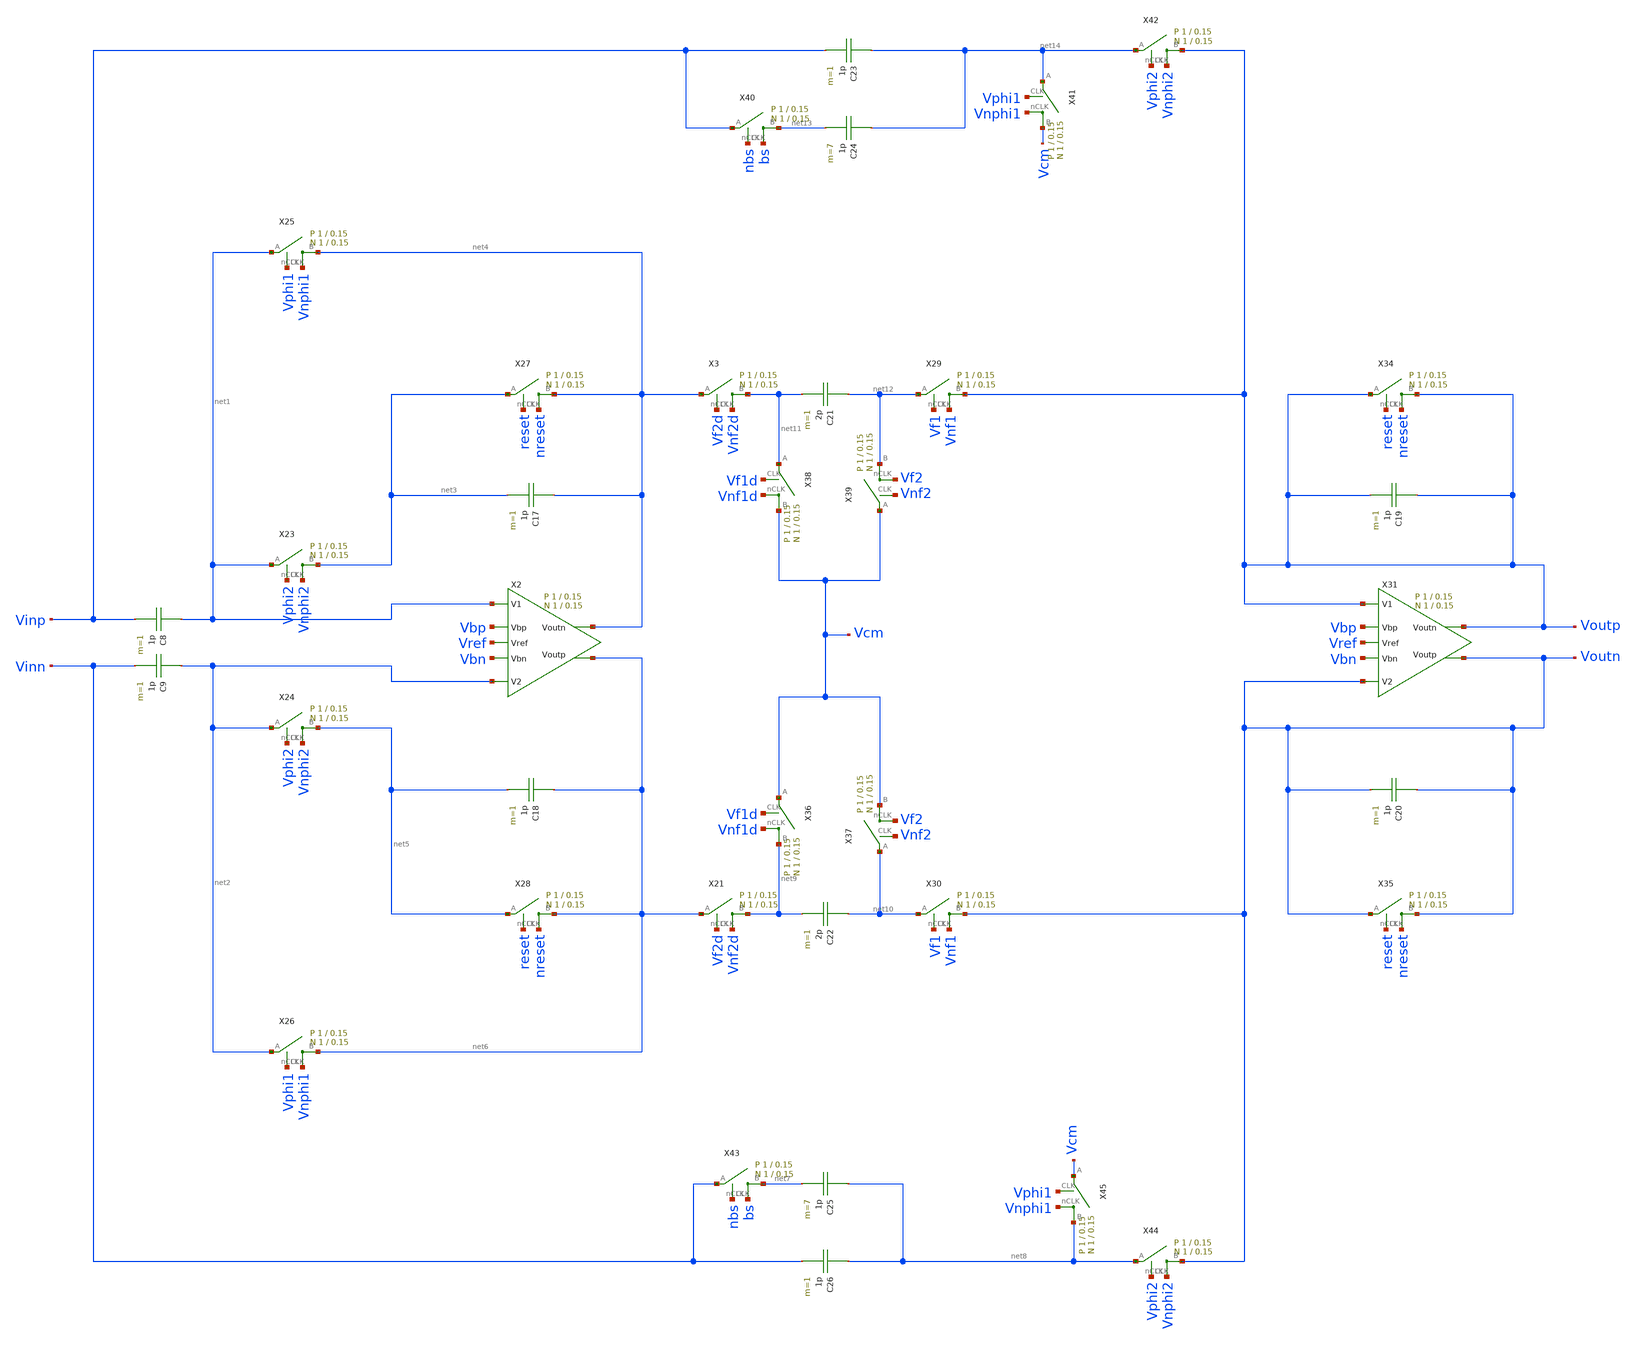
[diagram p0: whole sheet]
** sch_path: schematic/sigma_delta_modulator_simple_no_chop.sch
**.subckt sigma_delta_modulator_simple_no_chop
C8 net1 Vinp 1p m=1
C9 net2 Vinn 1p m=1
C17 net4 net3 1p m=1
C18 net6 net5 1p m=1
X23 net3 net1 Vphi2 Vnphi2 switch Wp=1 Lp=0.15 WW=1 LL=0.15
X24 net5 net2 Vphi2 Vnphi2 switch Wp=1 Lp=0.15 WW=1 LL=0.15
X25 net4 net1 Vphi1 Vnphi1 switch Wp=1 Lp=0.15 WW=1 LL=0.15
X26 net6 net2 Vphi1 Vnphi1 switch Wp=1 Lp=0.15 WW=1 LL=0.15
X27 net4 net3 reset nreset switch Wp=1 Lp=0.15 WW=1 LL=0.15
X28 net6 net5 reset nreset switch Wp=1 Lp=0.15 WW=1 LL=0.15
X3 net11 net4 Vf2d Vnf2d switch Wp=1 Lp=0.15 WW=1 LL=0.15
X21 net9 net6 Vf2d Vnf2d switch Wp=1 Lp=0.15 WW=1 LL=0.15
X29 Voutp net12 Vf1 Vnf1 switch Wp=1 Lp=0.15 WW=1 LL=0.15
X30 Voutn net10 Vf1 Vnf1 switch Wp=1 Lp=0.15 WW=1 LL=0.15
C19 Voutp Voutp 1p m=1
C20 Voutn Voutn 1p m=1
X34 Voutp Voutp reset nreset switch Wp=1 Lp=0.15 WW=1 LL=0.15
X35 Voutn Voutn reset nreset switch Wp=1 Lp=0.15 WW=1 LL=0.15
C21 net12 net11 2p m=1
C22 net10 net9 2p m=1
X36 net9 Vcm Vf1d Vnf1d switch Wp=1 Lp=0.15 WW=1 LL=0.15
X37 Vcm net10 Vnf2 Vf2 switch Wp=1 Lp=0.15 WW=1 LL=0.15
X38 Vcm net11 Vf1d Vnf1d switch Wp=1 Lp=0.15 WW=1 LL=0.15
X39 net12 Vcm Vnf2 Vf2 switch Wp=1 Lp=0.15 WW=1 LL=0.15
C23 net14 Vinp 1p m=1
C24 net14 net13 1p m=7
X40 net13 Vinp nbs bs switch Wp=1 Lp=0.15 WW=1 LL=0.15
X41 Vcm net14 Vphi1 Vnphi1 switch Wp=1 Lp=0.15 WW=1 LL=0.15
X42 Voutp net14 Vphi2 Vnphi2 switch Wp=1 Lp=0.15 WW=1 LL=0.15
C25 net8 net7 1p m=7
C26 net8 Vinn 1p m=1
X43 net7 Vinn nbs bs switch Wp=1 Lp=0.15 WW=1 LL=0.15
X44 Voutn net8 Vphi2 Vnphi2 switch Wp=1 Lp=0.15 WW=1 LL=0.15
X45 net8 Vcm Vphi1 Vnphi1 switch Wp=1 Lp=0.15 WW=1 LL=0.15
X2 net1 net2 net6 net4 Vbp Vref Vbn fully_differential_sc_amp Wp=1 Lp=0.15 WW=1 LL=0.15
X31 Voutp Voutn Voutn Voutp Vbp Vref Vbn fully_differential_sc_amp Wp=1 Lp=0.15 WW=1 LL=0.15
**.ends

* expanding   symbol:  /home/madvlsi/Documents/MADVLSI-Final_Project/schematic/switch.sym # of
*+ pins=4
** sym_path: schematic/switch.sym
** sch_path: schematic/switch.sch
.subckt switch B A CLK nCLK  Wp=1 Lp=0.15 WW=1 LL=0.15
*.iopin B
*.iopin A
*.ipin CLK
*.ipin nCLK
*.ipin CLK
*.ipin CLK
*.ipin nCLK
*.ipin nCLK
XM1 A CLK B GND sky130_fd_pr__nfet_01v8 L={LL} W={WW} nf=1 ad='int((nf+1)/2) * W/nf * 0.29' as='int((nf+2)/2) * W/nf * 0.29'
+ pd='2*int((nf+1)/2) * (W/nf + 0.29)' ps='2*int((nf+2)/2) * (W/nf + 0.29)' nrd='0.29 / W' nrs='0.29 / W'
+ sa=0 sb=0 sd=0 mult=1 m=1
XM2 A nCLK B VDD sky130_fd_pr__pfet_01v8 L={Lp} W={Wp} nf=1 ad='int((nf+1)/2) * W/nf * 0.29' as='int((nf+2)/2) * W/nf * 0.29'
+ pd='2*int((nf+1)/2) * (W/nf + 0.29)' ps='2*int((nf+2)/2) * (W/nf + 0.29)' nrd='0.29 / W' nrs='0.29 / W'
+ sa=0 sb=0 sd=0 mult=1 m=1
XM3 B CLK B VDD sky130_fd_pr__pfet_01v8 L={Lp} W={Wp/2} nf=1 ad='int((nf+1)/2) * W/nf * 0.29' as='int((nf+2)/2) * W/nf * 0.29'
+ pd='2*int((nf+1)/2) * (W/nf + 0.29)' ps='2*int((nf+2)/2) * (W/nf + 0.29)' nrd='0.29 / W' nrs='0.29 / W'
+ sa=0 sb=0 sd=0 mult=1 m=1
XM4 A CLK A VDD sky130_fd_pr__pfet_01v8 L={Lp} W={Wp/2} nf=1 ad='int((nf+1)/2) * W/nf * 0.29' as='int((nf+2)/2) * W/nf * 0.29'
+ pd='2*int((nf+1)/2) * (W/nf + 0.29)' ps='2*int((nf+2)/2) * (W/nf + 0.29)' nrd='0.29 / W' nrs='0.29 / W'
+ sa=0 sb=0 sd=0 mult=1 m=1
XM5 B nCLK B GND sky130_fd_pr__nfet_01v8 L={LL} W={WW/2} nf=1 ad='int((nf+1)/2) * W/nf * 0.29' as='int((nf+2)/2) * W/nf * 0.29'
+ pd='2*int((nf+1)/2) * (W/nf + 0.29)' ps='2*int((nf+2)/2) * (W/nf + 0.29)' nrd='0.29 / W' nrs='0.29 / W'
+ sa=0 sb=0 sd=0 mult=1 m=1
XM6 A nCLK A GND sky130_fd_pr__nfet_01v8 L={LL} W={WW/2} nf=1 ad='int((nf+1)/2) * W/nf * 0.29' as='int((nf+2)/2) * W/nf * 0.29'
+ pd='2*int((nf+1)/2) * (W/nf + 0.29)' ps='2*int((nf+2)/2) * (W/nf + 0.29)' nrd='0.29 / W' nrs='0.29 / W'
+ sa=0 sb=0 sd=0 mult=1 m=1
.ends


* expanding   symbol:
*+  /home/madvlsi/Documents/MADVLSI-Final_Project/schematic/fully_differential_sc_amp.sym # of pins=7
** sym_path: schematic/archive/fully_differential_sc_amp.sym
** sch_path: schematic/archive/fully_differential_sc_amp.sch
.subckt fully_differential_sc_amp V1 V2 Voutp Voutn Vbp Vref Vbn  Wp=1 Lp=0.15 WW=1 LL=0.15
*.ipin V1
*.ipin V2
*.ipin Vbp
*.ipin Vbn
*.ipin Vref
*.iopin Voutp
*.iopin Voutn
XM1a net2 V1 GND GND sky130_fd_pr__nfet_01v8 L=LL W=WW nf=1 ad='int((nf+1)/2) * W/nf * 0.29' as='int((nf+2)/2) * W/nf * 0.29'
+ pd='2*int((nf+1)/2) * (W/nf + 0.29)' ps='2*int((nf+2)/2) * (W/nf + 0.29)' nrd='0.29 / W' nrs='0.29 / W'
+ sa=0 sb=0 sd=0 mult=1 m=1
XM1b Voutn V1 GND GND sky130_fd_pr__nfet_01v8 L=LL W=WW nf=1 ad='int((nf+1)/2) * W/nf * 0.29' as='int((nf+2)/2) * W/nf * 0.29'
+ pd='2*int((nf+1)/2) * (W/nf + 0.29)' ps='2*int((nf+2)/2) * (W/nf + 0.29)' nrd='0.29 / W' nrs='0.29 / W'
+ sa=0 sb=0 sd=0 mult=1 m=1
XM2b Voutp V2 GND GND sky130_fd_pr__nfet_01v8 L=LL W=WW nf=1 ad='int((nf+1)/2) * W/nf * 0.29' as='int((nf+2)/2) * W/nf * 0.29'
+ pd='2*int((nf+1)/2) * (W/nf + 0.29)' ps='2*int((nf+2)/2) * (W/nf + 0.29)' nrd='0.29 / W' nrs='0.29 / W'
+ sa=0 sb=0 sd=0 mult=1 m=1
XM2a net2 V2 GND GND sky130_fd_pr__nfet_01v8 L=LL W=WW nf=1 ad='int((nf+1)/2) * W/nf * 0.29' as='int((nf+2)/2) * W/nf * 0.29'
+ pd='2*int((nf+1)/2) * (W/nf + 0.29)' ps='2*int((nf+2)/2) * (W/nf + 0.29)' nrd='0.29 / W' nrs='0.29 / W'
+ sa=0 sb=0 sd=0 mult=1 m=1
XMb net2 Vbp VDD VDD sky130_fd_pr__pfet_01v8 L=Lp W=Wp nf=1 ad='int((nf+1)/2) * W/nf * 0.29' as='int((nf+2)/2) * W/nf * 0.29'
+ pd='2*int((nf+1)/2) * (W/nf + 0.29)' ps='2*int((nf+2)/2) * (W/nf + 0.29)' nrd='0.29 / W' nrs='0.29 / W'
+ sa=0 sb=0 sd=0 mult=1 m=1
C2b net2 V2 1600f m=1
C2a net2 V1 1600f m=1
XM1 GND V2 net1 GND sky130_fd_pr__nfet_01v8 L=LL W=WW nf=1 ad='int((nf+1)/2) * W/nf * 0.29' as='int((nf+2)/2) * W/nf * 0.29'
+ pd='2*int((nf+1)/2) * (W/nf + 0.29)' ps='2*int((nf+2)/2) * (W/nf + 0.29)' nrd='0.29 / W' nrs='0.29 / W'
+ sa=0 sb=0 sd=0 mult=1 m=1
XM2 GND V1 net1 GND sky130_fd_pr__nfet_01v8 L=LL W=WW nf=1 ad='int((nf+1)/2) * W/nf * 0.29' as='int((nf+2)/2) * W/nf * 0.29'
+ pd='2*int((nf+1)/2) * (W/nf + 0.29)' ps='2*int((nf+2)/2) * (W/nf + 0.29)' nrd='0.29 / W' nrs='0.29 / W'
+ sa=0 sb=0 sd=0 mult=1 m=1
XMb1 VDD net4 net5 VDD sky130_fd_pr__pfet_01v8 L=Lp W=Wp nf=1 ad='int((nf+1)/2) * W/nf * 0.29' as='int((nf+2)/2) * W/nf * 0.29'
+ pd='2*int((nf+1)/2) * (W/nf + 0.29)' ps='2*int((nf+2)/2) * (W/nf + 0.29)' nrd='0.29 / W' nrs='0.29 / W'
+ sa=0 sb=0 sd=0 mult=1 m=1
XMb2 VDD net4 net1 VDD sky130_fd_pr__pfet_01v8 L=Lp W=Wp nf=1 ad='int((nf+1)/2) * W/nf * 0.29' as='int((nf+2)/2) * W/nf * 0.29'
+ pd='2*int((nf+1)/2) * (W/nf + 0.29)' ps='2*int((nf+2)/2) * (W/nf + 0.29)' nrd='0.29 / W' nrs='0.29 / W'
+ sa=0 sb=0 sd=0 mult=1 m=1
XMb4 VDD net4 net6 VDD sky130_fd_pr__pfet_01v8 L=Lp W=Wp nf=1 ad='int((nf+1)/2) * W/nf * 0.29' as='int((nf+2)/2) * W/nf * 0.29'
+ pd='2*int((nf+1)/2) * (W/nf + 0.29)' ps='2*int((nf+2)/2) * (W/nf + 0.29)' nrd='0.29 / W' nrs='0.29 / W'
+ sa=0 sb=0 sd=0 mult=1 m=1
XMb5 net7 net4 VDD VDD sky130_fd_pr__pfet_01v8 L=Lp W=Wp nf=1 ad='int((nf+1)/2) * W/nf * 0.29' as='int((nf+2)/2) * W/nf * 0.29'
+ pd='2*int((nf+1)/2) * (W/nf + 0.29)' ps='2*int((nf+2)/2) * (W/nf + 0.29)' nrd='0.29 / W' nrs='0.29 / W'
+ sa=0 sb=0 sd=0 mult=1 m=1
XM3 net3 Vbn GND GND sky130_fd_pr__nfet_01v8 L=LL W=WW nf=1 ad='int((nf+1)/2) * W/nf * 0.29' as='int((nf+2)/2) * W/nf * 0.29'
+ pd='2*int((nf+1)/2) * (W/nf + 0.29)' ps='2*int((nf+2)/2) * (W/nf + 0.29)' nrd='0.29 / W' nrs='0.29 / W'
+ sa=0 sb=0 sd=0 mult=1 m=1
XM4 VDD net1 net3 GND sky130_fd_pr__nfet_01v8 L=LL W=WW nf=1 ad='int((nf+1)/2) * W/nf * 0.29' as='int((nf+2)/2) * W/nf * 0.29'
+ pd='2*int((nf+1)/2) * (W/nf + 0.29)' ps='2*int((nf+2)/2) * (W/nf + 0.29)' nrd='0.29 / W' nrs='0.29 / W'
+ sa=0 sb=0 sd=0 mult=1 m=1
XM5 net3 Vref net4 GND sky130_fd_pr__nfet_01v8 L=LL W=WW nf=1 ad='int((nf+1)/2) * W/nf * 0.29' as='int((nf+2)/2) * W/nf * 0.29'
+ pd='2*int((nf+1)/2) * (W/nf + 0.29)' ps='2*int((nf+2)/2) * (W/nf + 0.29)' nrd='0.29 / W' nrs='0.29 / W'
+ sa=0 sb=0 sd=0 mult=1 m=1
XMb6 net5 net4 Voutn VDD sky130_fd_pr__pfet_01v8 L=Lp W=Wp nf=1 ad='int((nf+1)/2) * W/nf * 0.29' as='int((nf+2)/2) * W/nf * 0.29'
+ pd='2*int((nf+1)/2) * (W/nf + 0.29)' ps='2*int((nf+2)/2) * (W/nf + 0.29)' nrd='0.29 / W' nrs='0.29 / W'
+ sa=0 sb=0 sd=0 mult=1 m=1
XMb7 net6 net4 Voutp VDD sky130_fd_pr__pfet_01v8 L=Lp W=Wp nf=1 ad='int((nf+1)/2) * W/nf * 0.29' as='int((nf+2)/2) * W/nf * 0.29'
+ pd='2*int((nf+1)/2) * (W/nf + 0.29)' ps='2*int((nf+2)/2) * (W/nf + 0.29)' nrd='0.29 / W' nrs='0.29 / W'
+ sa=0 sb=0 sd=0 mult=1 m=1
XMb8 net4 net4 net7 VDD sky130_fd_pr__pfet_01v8 L=Lp W=Wp nf=1 ad='int((nf+1)/2) * W/nf * 0.29' as='int((nf+2)/2) * W/nf * 0.29'
+ pd='2*int((nf+1)/2) * (W/nf + 0.29)' ps='2*int((nf+2)/2) * (W/nf + 0.29)' nrd='0.29 / W' nrs='0.29 / W'
+ sa=0 sb=0 sd=0 mult=1 m=1
.ends

.GLOBAL VDD
.GLOBAL GND
.end
